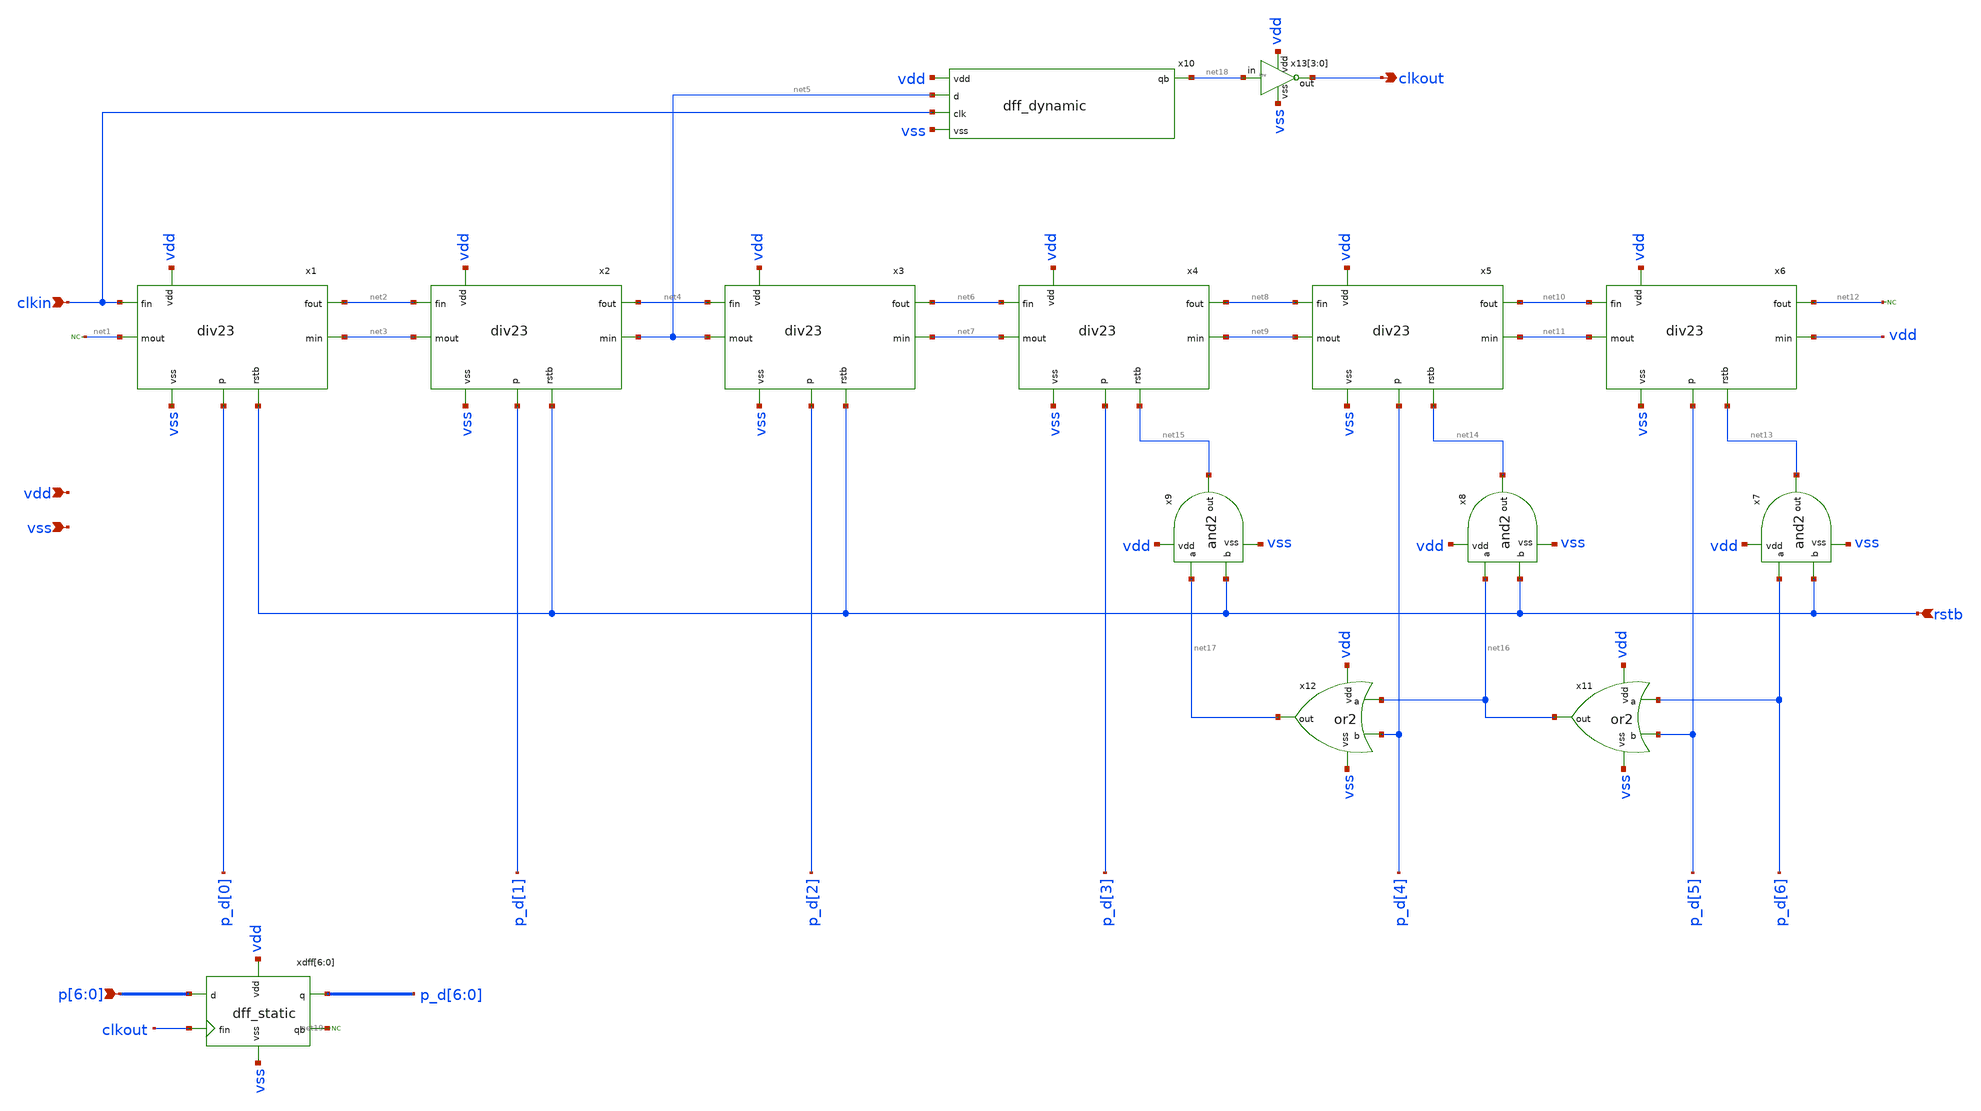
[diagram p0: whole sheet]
** sch_path: xschem/mmd.sch
**.subckt mmd clkin p[6],p[5],p[4],p[3],p[2],p[1],p[0] clkout rstb vdd vss
*.ipin clkin
*.ipin p[6],p[5],p[4],p[3],p[2],p[1],p[0]
*.opin clkout
*.ipin rstb
*.ipin vdd
*.ipin vss
x1 vdd vss clkin net2 net1 rstb p_d[0] net3 div23
x2 vdd vss net2 net4 net3 rstb p_d[1] net5 div23
x3 vdd vss net4 net6 net5 rstb p_d[2] net7 div23
x4 vdd vss net6 net8 net7 net15 p_d[3] net9 div23
x5 vdd vss net8 net10 net9 net14 p_d[4] net11 div23
x6 vdd vss net10 net12 net11 net13 p_d[5] vdd div23
x7 vdd p_d[6] rstb net13 vss and2
x8 vdd net16 rstb net14 vss and2
x9 vdd net17 rstb net15 vss and2
x11 vdd p_d[6] p_d[5] net16 vss or2
x12 vdd net16 p_d[4] net17 vss or2
* noconn #net12
* noconn #net1
x10 net18 net5 vdd vss clkin dff_dynamic
xdff[6] vdd net19[6] p_d[6] clkout p[6] vss dff_static
xdff[5] vdd net19[5] p_d[5] clkout p[5] vss dff_static
xdff[4] vdd net19[4] p_d[4] clkout p[4] vss dff_static
xdff[3] vdd net19[3] p_d[3] clkout p[3] vss dff_static
xdff[2] vdd net19[2] p_d[2] clkout p[2] vss dff_static
xdff[1] vdd net19[1] p_d[1] clkout p[1] vss dff_static
xdff[0] vdd net19[0] p_d[0] clkout p[0] vss dff_static
x13[3] vdd net18 clkout vss inv
x13[2] vdd net18 clkout vss inv
x13[1] vdd net18 clkout vss inv
x13[0] vdd net18 clkout vss inv
* noconn #net19
**.ends
.end
